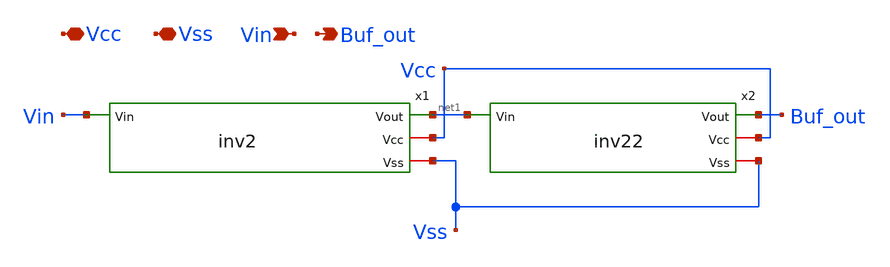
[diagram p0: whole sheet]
** sch_path: Git Files/Schematic/Pre Emphasis Driver/buf2.sch
**.subckt buf2 Vcc Vss Vin Buf_out
*.iopin Vcc
*.iopin Vss
*.ipin Vin
*.opin Buf_out
x1 Vin net1 Vcc Vss inv2
x2 net1 Buf_out Vcc Vss inv22
**.ends
.end
